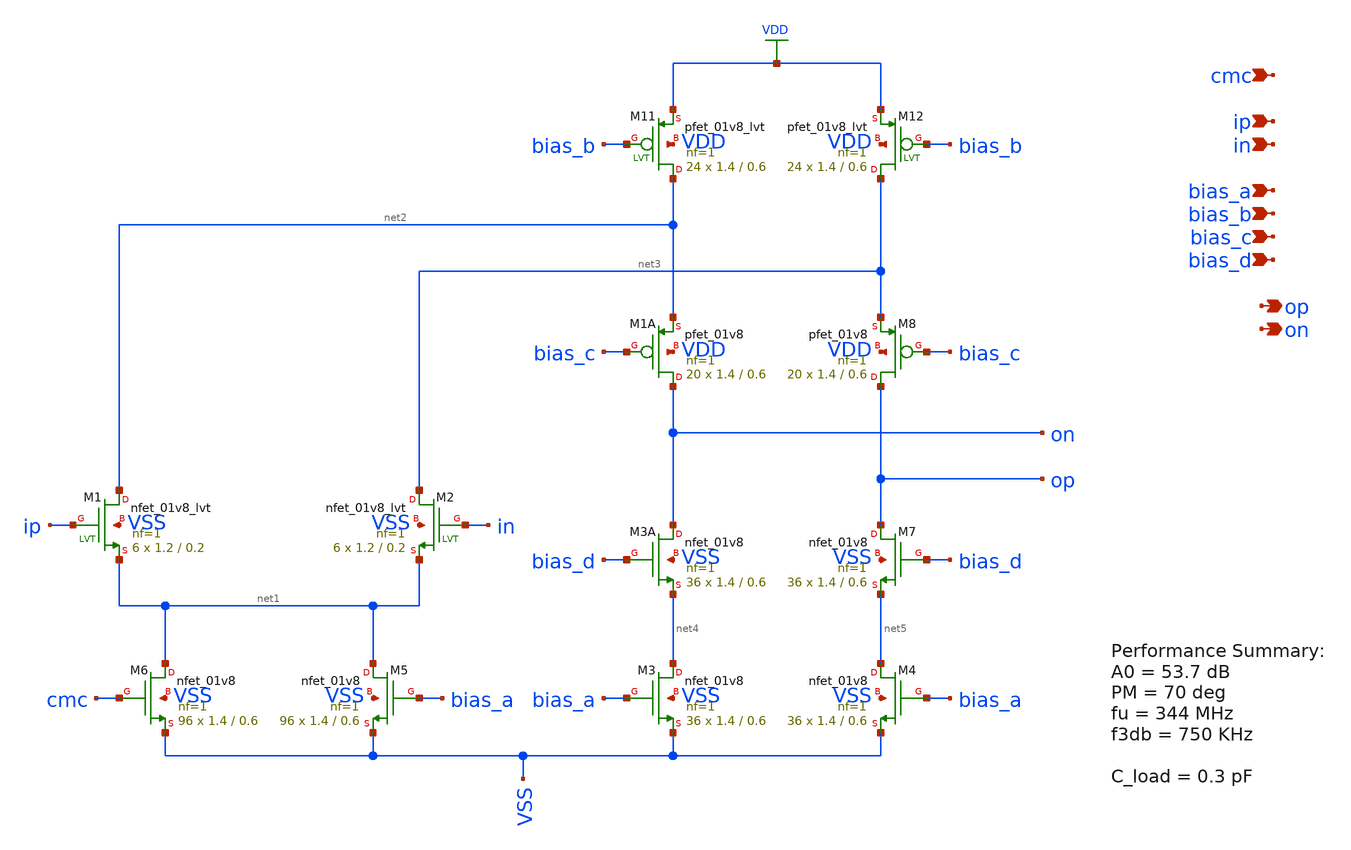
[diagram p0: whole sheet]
** sch_path: design/schematic/folded_cascode_3_core.sch
**.subckt folded_cascode_3_core cmc ip in bias_a bias_b bias_c bias_d op on
*.ipin cmc
*.ipin ip
*.ipin in
*.ipin bias_a
*.ipin bias_b
*.ipin bias_c
*.ipin bias_d
*.opin op
*.opin on
XM1 net2 ip net1 VSS sky130_fd_pr__nfet_01v8_lvt L=0.2 W=1.2 nf=1 ad='int((nf+1)/2) * W/nf * 0.29' as='int((nf+2)/2) * W/nf * 0.29'
+ pd='2*int((nf+1)/2) * (W/nf + 0.29)' ps='2*int((nf+2)/2) * (W/nf + 0.29)' nrd='0.29 / W' nrs='0.29 / W'
+ sa=0 sb=0 sd=0 mult=6 m=6
XM2 net3 in net1 VSS sky130_fd_pr__nfet_01v8_lvt L=0.2 W=1.2 nf=1 ad='int((nf+1)/2) * W/nf * 0.29' as='int((nf+2)/2) * W/nf * 0.29'
+ pd='2*int((nf+1)/2) * (W/nf + 0.29)' ps='2*int((nf+2)/2) * (W/nf + 0.29)' nrd='0.29 / W' nrs='0.29 / W'
+ sa=0 sb=0 sd=0 mult=6 m=6
XM6 net1 cmc VSS VSS sky130_fd_pr__nfet_01v8 L=0.6 W=1.4 nf=1 ad='int((nf+1)/2) * W/nf * 0.29' as='int((nf+2)/2) * W/nf * 0.29'
+ pd='2*int((nf+1)/2) * (W/nf + 0.29)' ps='2*int((nf+2)/2) * (W/nf + 0.29)' nrd='0.29 / W' nrs='0.29 / W'
+ sa=0 sb=0 sd=0 mult=96 m=96
XM5 net1 bias_a VSS VSS sky130_fd_pr__nfet_01v8 L=0.6 W=1.4 nf=1 ad='int((nf+1)/2) * W/nf * 0.29' as='int((nf+2)/2) * W/nf * 0.29'
+ pd='2*int((nf+1)/2) * (W/nf + 0.29)' ps='2*int((nf+2)/2) * (W/nf + 0.29)' nrd='0.29 / W' nrs='0.29 / W'
+ sa=0 sb=0 sd=0 mult=96 m=96
XM11 net2 bias_b VDD VDD sky130_fd_pr__pfet_01v8_lvt L=0.6 W=1.4 nf=1 ad='int((nf+1)/2) * W/nf * 0.29'
+ as='int((nf+2)/2) * W/nf * 0.29' pd='2*int((nf+1)/2) * (W/nf + 0.29)' ps='2*int((nf+2)/2) * (W/nf + 0.29)'
+ nrd='0.29 / W' nrs='0.29 / W' sa=0 sb=0 sd=0 mult=24 m=24
XM12 net3 bias_b VDD VDD sky130_fd_pr__pfet_01v8_lvt L=0.6 W=1.4 nf=1 ad='int((nf+1)/2) * W/nf * 0.29'
+ as='int((nf+2)/2) * W/nf * 0.29' pd='2*int((nf+1)/2) * (W/nf + 0.29)' ps='2*int((nf+2)/2) * (W/nf + 0.29)'
+ nrd='0.29 / W' nrs='0.29 / W' sa=0 sb=0 sd=0 mult=24 m=24
XM1A on bias_c net2 VDD sky130_fd_pr__pfet_01v8 L=0.6 W=1.4 nf=1 ad='int((nf+1)/2) * W/nf * 0.29' as='int((nf+2)/2) * W/nf * 0.29'
+ pd='2*int((nf+1)/2) * (W/nf + 0.29)' ps='2*int((nf+2)/2) * (W/nf + 0.29)' nrd='0.29 / W' nrs='0.29 / W'
+ sa=0 sb=0 sd=0 mult=20 m=20
XM8 op bias_c net3 VDD sky130_fd_pr__pfet_01v8 L=0.6 W=1.4 nf=1 ad='int((nf+1)/2) * W/nf * 0.29' as='int((nf+2)/2) * W/nf * 0.29'
+ pd='2*int((nf+1)/2) * (W/nf + 0.29)' ps='2*int((nf+2)/2) * (W/nf + 0.29)' nrd='0.29 / W' nrs='0.29 / W'
+ sa=0 sb=0 sd=0 mult=20 m=20
XM3A on bias_d net4 VSS sky130_fd_pr__nfet_01v8 L=0.6 W=1.4 nf=1 ad='int((nf+1)/2) * W/nf * 0.29' as='int((nf+2)/2) * W/nf * 0.29'
+ pd='2*int((nf+1)/2) * (W/nf + 0.29)' ps='2*int((nf+2)/2) * (W/nf + 0.29)' nrd='0.29 / W' nrs='0.29 / W'
+ sa=0 sb=0 sd=0 mult=36 m=36
XM7 op bias_d net5 VSS sky130_fd_pr__nfet_01v8 L=0.6 W=1.4 nf=1 ad='int((nf+1)/2) * W/nf * 0.29' as='int((nf+2)/2) * W/nf * 0.29'
+ pd='2*int((nf+1)/2) * (W/nf + 0.29)' ps='2*int((nf+2)/2) * (W/nf + 0.29)' nrd='0.29 / W' nrs='0.29 / W'
+ sa=0 sb=0 sd=0 mult=36 m=36
XM3 net4 bias_a VSS VSS sky130_fd_pr__nfet_01v8 L=0.6 W=1.4 nf=1 ad='int((nf+1)/2) * W/nf * 0.29' as='int((nf+2)/2) * W/nf * 0.29'
+ pd='2*int((nf+1)/2) * (W/nf + 0.29)' ps='2*int((nf+2)/2) * (W/nf + 0.29)' nrd='0.29 / W' nrs='0.29 / W'
+ sa=0 sb=0 sd=0 mult=36 m=36
XM4 net5 bias_a VSS VSS sky130_fd_pr__nfet_01v8 L=0.6 W=1.4 nf=1 ad='int((nf+1)/2) * W/nf * 0.29' as='int((nf+2)/2) * W/nf * 0.29'
+ pd='2*int((nf+1)/2) * (W/nf + 0.29)' ps='2*int((nf+2)/2) * (W/nf + 0.29)' nrd='0.29 / W' nrs='0.29 / W'
+ sa=0 sb=0 sd=0 mult=36 m=36
**.ends
.GLOBAL VDD
.end
